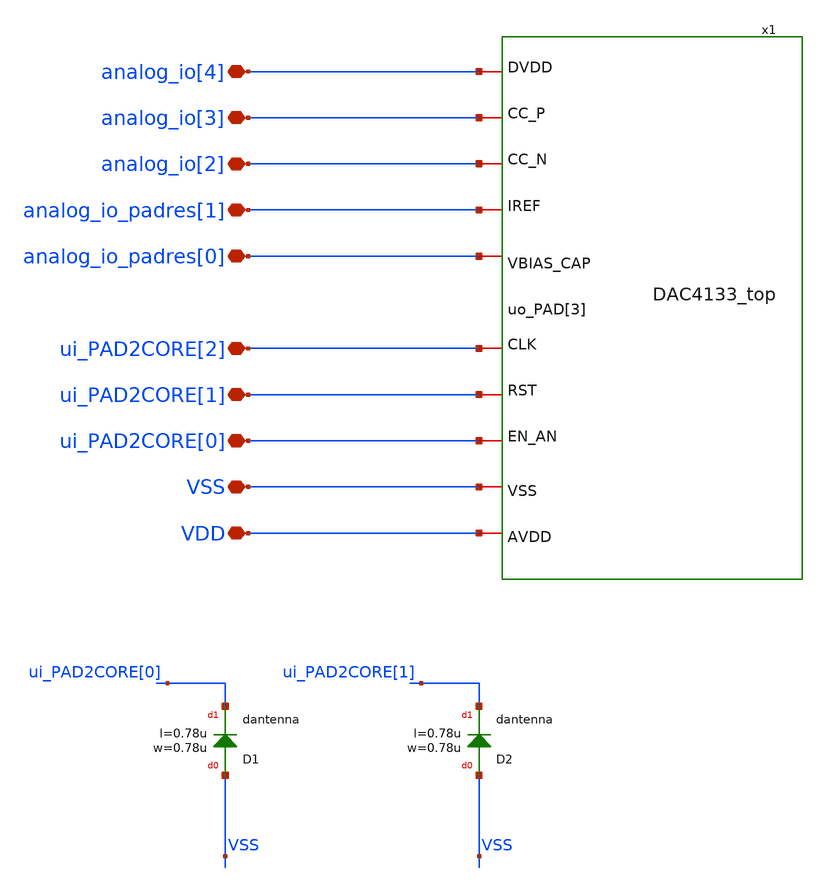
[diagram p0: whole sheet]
** sch_path: DAC4133-main/schematic/xschem/DAC4133.sch
**.subckt DAC4133 VSS VDD ui_PAD2CORE[1] ui_PAD2CORE[0] ui_PAD2CORE[2] analog_io_padres[1]
*+ analog_io_padres[0] analog_io[3] analog_io[2] analog_io[4]
*.iopin VSS
*.iopin VDD
*.iopin ui_PAD2CORE[1]
*.iopin ui_PAD2CORE[0]
*.iopin ui_PAD2CORE[2]
*.iopin analog_io_padres[1]
*.iopin analog_io_padres[0]
*.iopin analog_io[3]
*.iopin analog_io[2]
*.iopin analog_io[4]
x1 ui_PAD2CORE[0] ui_PAD2CORE[1] ui_PAD2CORE[2] analog_io_padres[0] analog_io_padres[1] analog_io[2]
+ analog_io[3] analog_io[4] VDD VSS DAC4133_top
XD1 VSS ui_PAD2CORE[0] dantenna l=0.78u w=0.78u
XD2 VSS ui_PAD2CORE[1] dantenna l=0.78u w=0.78u
**.ends
.end
